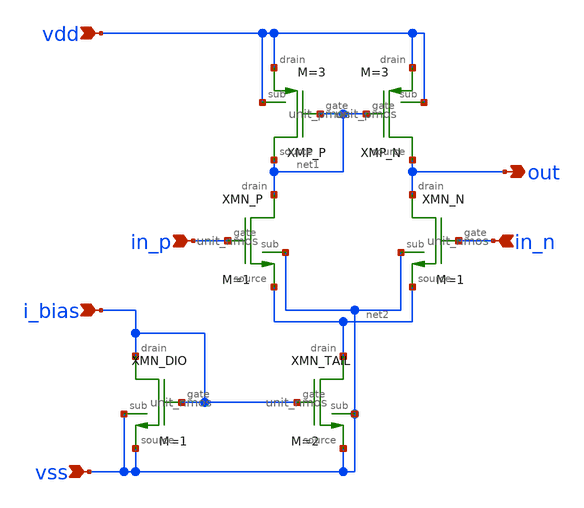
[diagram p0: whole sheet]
** sch_path: designs/libs/core_analog/ota_5t/ota_5t.sch
**.subckt ota_5t in_p in_n i_bias vdd vss out
*.ipin in_p
*.ipin in_n
*.ipin i_bias
*.ipin vdd
*.ipin vss
*.opin out
XMN_TAIL net2 vss i_bias vss unit_nmos M=2
XMP_N vdd vdd net1 out unit_pmos M=3
XMN_DIO i_bias vss i_bias vss unit_nmos M=1
XMP_P vdd vdd net1 net1 unit_pmos M=3
XMN_P net1 vss in_p net2 unit_nmos M=1
XMN_N out vss in_n net2 unit_nmos M=1
**.ends
.end
